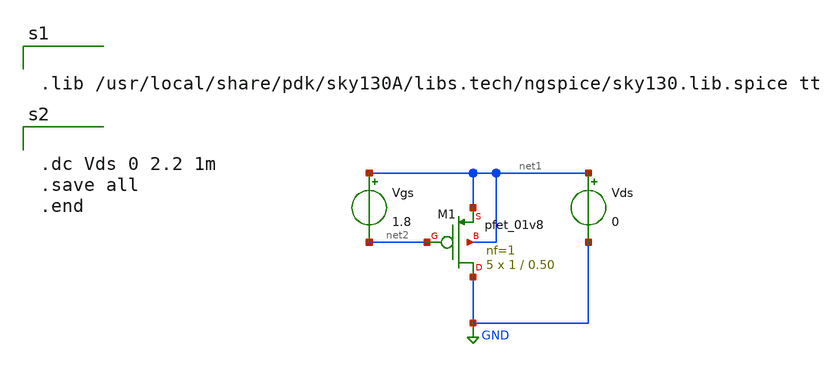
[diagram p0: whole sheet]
** sch_path: xschem files/pmos_char_1v8.sch
**.subckt pmos_char_1v8
XM1 GND net2 net1 net1 sky130_fd_pr__pfet_01v8 L=0.50 W=1 nf=1 ad='int((nf+1)/2) * W/nf * 0.29' as='int((nf+2)/2) * W/nf * 0.29'
+ pd='2*int((nf+1)/2) * (W/nf + 0.29)' ps='2*int((nf+2)/2) * (W/nf + 0.29)' nrd='0.29 / W' nrs='0.29 / W'
+ sa=0 sb=0 sd=0 mult=5 m=5
Vgs net1 net2 1.8
Vds net1 GND 0
**** begin user architecture code


.lib /usr/local/share/pdk/sky130A/libs.tech/ngspice/sky130.lib.spice tt



.dc Vds 0 2.2 1m
.save all
.end


**** end user architecture code
**.ends
.GLOBAL GND
.end
